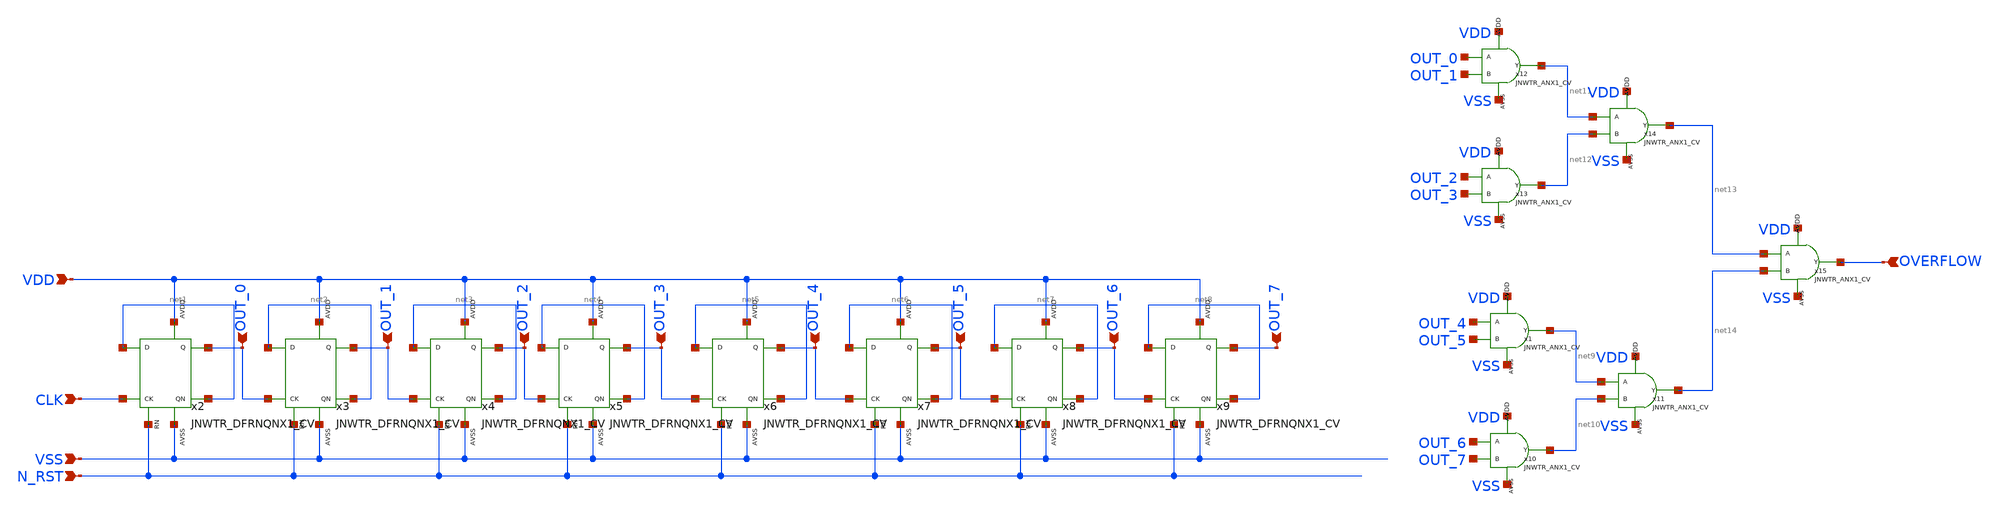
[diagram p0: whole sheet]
** sch_path: design/JNW_GR02_SKY130A/JNW_GR02_COUNTER.sch
**.subckt JNW_GR02_COUNTER CLK VDD N_RST OVERFLOW OUT_7 OUT_6 OUT_5 OUT_4 OUT_3 OUT_2 OUT_1 OUT_0
*+ VSS
*.ipin CLK
*.ipin VDD
*.ipin N_RST
*.ipin OVERFLOW
*.ipin OUT_7
*.ipin OUT_6
*.ipin OUT_5
*.ipin OUT_4
*.ipin OUT_3
*.ipin OUT_2
*.ipin OUT_1
*.ipin OUT_0
*.ipin VSS
x2 net1 CLK N_RST OUT_0 net1 VDD VSS JNWTR_DFRNQNX1_CV xoffset=0 yoffset=0 angle=0
x3 net2 OUT_0 N_RST OUT_1 net2 VDD VSS JNWTR_DFRNQNX1_CV xoffset=0 yoffset=0 angle=0
x4 net3 OUT_1 N_RST OUT_2 net3 VDD VSS JNWTR_DFRNQNX1_CV xoffset=0 yoffset=0 angle=0
x5 net4 OUT_2 N_RST OUT_3 net4 VDD VSS JNWTR_DFRNQNX1_CV xoffset=0 yoffset=0 angle=0
x6 net5 OUT_3 N_RST OUT_4 net5 VDD VSS JNWTR_DFRNQNX1_CV xoffset=0 yoffset=0 angle=0
x7 net6 OUT_4 N_RST OUT_5 net6 VDD VSS JNWTR_DFRNQNX1_CV xoffset=0 yoffset=0 angle=0
x8 net7 OUT_5 N_RST OUT_6 net7 VDD VSS JNWTR_DFRNQNX1_CV xoffset=0 yoffset=0 angle=0
x9 net8 OUT_6 N_RST OUT_7 net8 VDD VSS JNWTR_DFRNQNX1_CV xoffset=0 yoffset=0 angle=0
x1 OUT_4 OUT_5 net9 VDD VSS JNWTR_ANX1_CV xoffset=0 yoffset=0 angle=0 M=1
x10 OUT_6 OUT_7 net10 VDD VSS JNWTR_ANX1_CV xoffset=0 yoffset=0 angle=0 M=1
x11 net9 net10 net14 VDD VSS JNWTR_ANX1_CV xoffset=0 yoffset=0 angle=0 M=1
x12 OUT_0 OUT_1 net11 VDD VSS JNWTR_ANX1_CV xoffset=0 yoffset=0 angle=0 M=1
x13 OUT_2 OUT_3 net12 VDD VSS JNWTR_ANX1_CV xoffset=0 yoffset=0 angle=0 M=1
x14 net11 net12 net13 VDD VSS JNWTR_ANX1_CV xoffset=0 yoffset=0 angle=0 M=1
x15 net13 net14 OVERFLOW VDD VSS JNWTR_ANX1_CV xoffset=0 yoffset=0 angle=0 M=1
**.ends
.end
